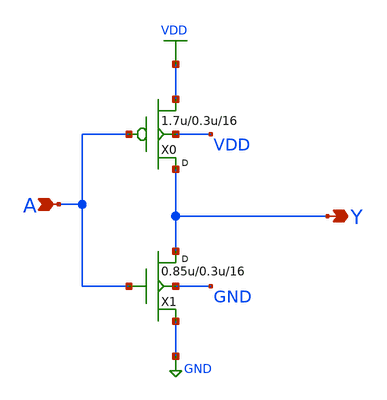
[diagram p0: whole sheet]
** sch_path: gf180mcu_osu_sc_gp9t3v3/cells/clkinv/gf180mcu_osu_sc_gp9t3v3__clkinv_16.sch
**.subckt gf180mcu_osu_sc_gp9t3v3__clkinv_16 A Y
*.ipin A
*.opin Y
X0 Y A VDD VDD pmos_3p3 w=1.7u l=0.3u m=16
X1 Y A GND GND nmos_3p3 w=0.85u l=0.3u m=16
**.ends
.GLOBAL VDD
.GLOBAL GND
.end
